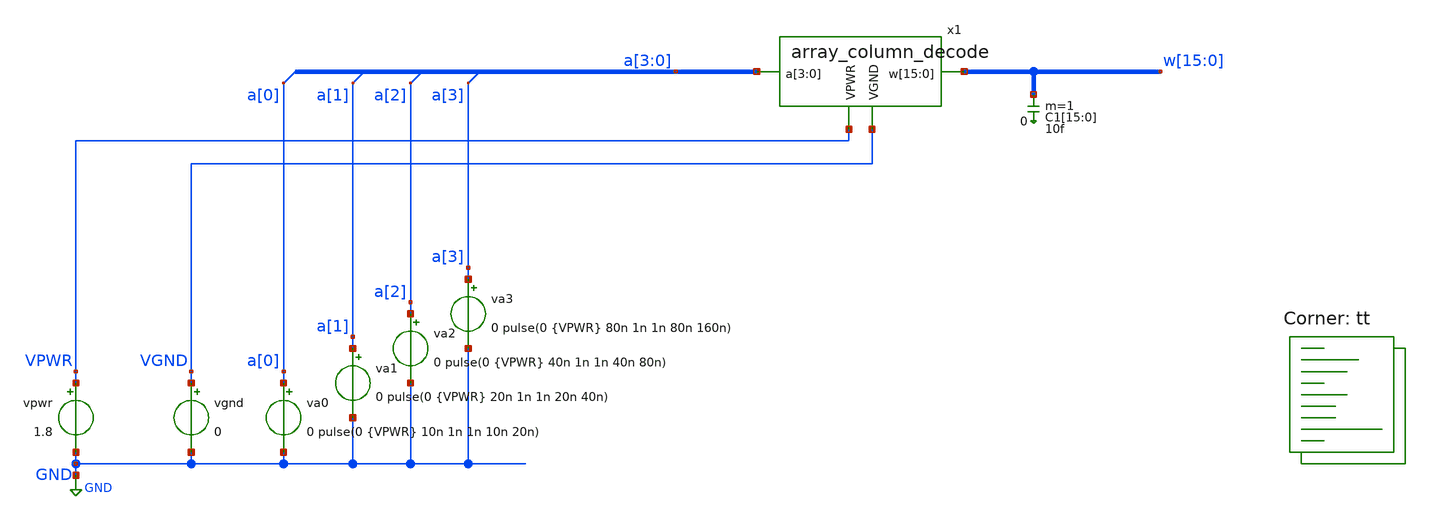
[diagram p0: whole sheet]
** sch_path: xschem/test_array_column_decode.sch
**.subckt test_array_column_decode
vpwr VPWR GND 1.8
va0 a[0] GND 0 pulse(0 {VPWR} 10n 1n 1n 10n 20n)
vgnd VGND GND 0
va1 a[1] GND 0 pulse(0 {VPWR} 20n 1n 1n 20n 40n)
va2 a[2] GND 0 pulse(0 {VPWR} 40n 1n 1n 40n 80n)
va3 a[3] GND 0 pulse(0 {VPWR} 80n 1n 1n 80n 160n)
C1[15] w[15] 0 10f m=1
C1[14] w[14] 0 10f m=1
C1[13] w[13] 0 10f m=1
C1[12] w[12] 0 10f m=1
C1[11] w[11] 0 10f m=1
C1[10] w[10] 0 10f m=1
C1[9] w[9] 0 10f m=1
C1[8] w[8] 0 10f m=1
C1[7] w[7] 0 10f m=1
C1[6] w[6] 0 10f m=1
C1[5] w[5] 0 10f m=1
C1[4] w[4] 0 10f m=1
C1[3] w[3] 0 10f m=1
C1[2] w[2] 0 10f m=1
C1[1] w[1] 0 10f m=1
C1[0] w[0] 0 10f m=1
x1 VPWR VGND a[3] a[2] a[1] a[0] w[15] w[14] w[13] w[12] w[11] w[10] w[9] w[8] w[7] w[6] w[5] w[4]
+ w[3] w[2] w[1] w[0] array_column_decode
**** begin user architecture code
.lib $::SKYWATER_MODELS/sky130.lib.spice tt



.param VPWR=1.8
.param VSS=0
.options savecurrents
.control
  save all
  op
  remzerovec
  write test_array_column_decode.raw
  set appendwrite
  * tran
  tran 1n 1u
  remzerovec
  write test_array_column_decode.raw
.endc



**** end user architecture code
**.ends

* expanding   symbol:  array_column_decode.sym # of pins=4
** sym_path: xschem/array_column_decode.sym
** sch_path: xschem/array_column_decode.sch
.subckt array_column_decode VPWR VGND a[3] a[2] a[1] a[0] w[15] w[14] w[13] w[12] w[11] w[10] w[9]
+ w[8] w[7] w[6] w[5] w[4] w[3] w[2] w[1] w[0]
*.ipin a[3],a[2],a[1],a[0]
*.ipin VPWR
*.ipin VGND
*.opin w[15],w[14],w[13],w[12],w[11],w[10],w[9],w[8],w[7],w[6],w[5],w[4],w[3],w[2],w[1],w[0]
**** begin user architecture code
 .lib $::SKYWATER_MODELS/sky130.lib.spice tt

.include $::SKYWATER_STDCELLS/sky130_fd_sc_hd.spice



**** end user architecture code
x2 a[3] VGND VGND VPWR VPWR a[3]_b sky130_fd_sc_hd__inv_1
x3 a[2] VGND VGND VPWR VPWR a[2]_b sky130_fd_sc_hd__inv_1
x4 a[1] VGND VGND VPWR VPWR a[1]_b sky130_fd_sc_hd__inv_1
x5 a[0] VGND VGND VPWR VPWR a[0]_b sky130_fd_sc_hd__inv_1
x13 a[2] a[3] VGND VGND VPWR VPWR net8 sky130_fd_sc_hd__nand2_2
x6 a[0]_b a[1]_b VGND VGND VPWR VPWR net1 sky130_fd_sc_hd__nand2_2
x7 a[0] a[1]_b VGND VGND VPWR VPWR net3 sky130_fd_sc_hd__nand2_2
x8 a[0]_b a[1] VGND VGND VPWR VPWR net4 sky130_fd_sc_hd__nand2_2
x9 a[0] a[1] VGND VGND VPWR VPWR net5 sky130_fd_sc_hd__nand2_2
x10 a[2]_b a[3]_b VGND VGND VPWR VPWR net2 sky130_fd_sc_hd__nand2_2
x11 a[2] a[3]_b VGND VGND VPWR VPWR net6 sky130_fd_sc_hd__nand2_2
x12 a[2]_b a[3] VGND VGND VPWR VPWR net7 sky130_fd_sc_hd__nand2_2
x14 net1 net2 VGND VGND VGND VPWR VPWR w[0] sky130_fd_sc_hd__nor3_1
x15 net3 net2 VGND VGND VGND VPWR VPWR w[1] sky130_fd_sc_hd__nor3_1
x16 net4 net2 VGND VGND VGND VPWR VPWR w[2] sky130_fd_sc_hd__nor3_1
x17 net5 net2 VGND VGND VGND VPWR VPWR w[3] sky130_fd_sc_hd__nor3_1
x18 net1 net6 VGND VGND VGND VPWR VPWR w[4] sky130_fd_sc_hd__nor3_1
x19 net3 net6 VGND VGND VGND VPWR VPWR w[5] sky130_fd_sc_hd__nor3_1
x20 net4 net6 VGND VGND VGND VPWR VPWR w[6] sky130_fd_sc_hd__nor3_1
x21 net5 net6 VGND VGND VGND VPWR VPWR w[7] sky130_fd_sc_hd__nor3_1
x22 net1 net7 VGND VGND VGND VPWR VPWR w[8] sky130_fd_sc_hd__nor3_1
x23 net3 net7 VGND VGND VGND VPWR VPWR w[9] sky130_fd_sc_hd__nor3_1
x24 net4 net7 VGND VGND VGND VPWR VPWR w[10] sky130_fd_sc_hd__nor3_1
x25 net5 net7 VGND VGND VGND VPWR VPWR w[11] sky130_fd_sc_hd__nor3_1
x26 net1 net8 VGND VGND VGND VPWR VPWR w[12] sky130_fd_sc_hd__nor3_1
x27 net3 net8 VGND VGND VGND VPWR VPWR w[13] sky130_fd_sc_hd__nor3_1
x28 net4 net8 VGND VGND VGND VPWR VPWR w[14] sky130_fd_sc_hd__nor3_1
x29 net5 net8 VGND VGND VGND VPWR VPWR w[15] sky130_fd_sc_hd__nor3_1
x46 VGND VPWR sky130_fd_sc_hd__tapvpwrvgnd_1
x47 VGND VGND VPWR VPWR sky130_fd_sc_hd__decap_3
x48 VGND VPWR sky130_fd_sc_hd__tapvpwrvgnd_1
x49 VGND VPWR sky130_fd_sc_hd__tapvpwrvgnd_1
x50 VGND VGND VPWR VPWR sky130_fd_sc_hd__decap_3
x51 VGND VPWR sky130_fd_sc_hd__tapvpwrvgnd_1
x52 VGND VPWR sky130_fd_sc_hd__tapvpwrvgnd_1
x53 VGND VGND VPWR VPWR sky130_fd_sc_hd__decap_3
x54 VGND VPWR sky130_fd_sc_hd__tapvpwrvgnd_1
x55 VGND VPWR sky130_fd_sc_hd__tapvpwrvgnd_1
x56 VGND VGND VPWR VPWR sky130_fd_sc_hd__decap_3
x57 VGND VPWR sky130_fd_sc_hd__tapvpwrvgnd_1
x58 VGND VPWR sky130_fd_sc_hd__tapvpwrvgnd_1
x59 VGND VGND VPWR VPWR sky130_fd_sc_hd__decap_3
x60 VGND VPWR sky130_fd_sc_hd__tapvpwrvgnd_1
x61 VGND VPWR sky130_fd_sc_hd__tapvpwrvgnd_1
x62 VGND VGND VPWR VPWR sky130_fd_sc_hd__decap_3
x63 VGND VPWR sky130_fd_sc_hd__tapvpwrvgnd_1
x64 VGND VPWR sky130_fd_sc_hd__tapvpwrvgnd_1
x65 VGND VGND VPWR VPWR sky130_fd_sc_hd__decap_3
x66 VGND VPWR sky130_fd_sc_hd__tapvpwrvgnd_1
x67 VGND VPWR sky130_fd_sc_hd__tapvpwrvgnd_1
x68 VGND VGND VPWR VPWR sky130_fd_sc_hd__decap_3
x69 VGND VPWR sky130_fd_sc_hd__tapvpwrvgnd_1
x70 VGND VPWR sky130_fd_sc_hd__tapvpwrvgnd_1
x71 VGND VGND VPWR VPWR sky130_fd_sc_hd__decap_3
x72 VGND VPWR sky130_fd_sc_hd__tapvpwrvgnd_1
x73 VGND VPWR sky130_fd_sc_hd__tapvpwrvgnd_1
x74 VGND VGND VPWR VPWR sky130_fd_sc_hd__decap_3
x75 VGND VPWR sky130_fd_sc_hd__tapvpwrvgnd_1
x76 VGND VPWR sky130_fd_sc_hd__tapvpwrvgnd_1
x77 VGND VGND VPWR VPWR sky130_fd_sc_hd__decap_3
x78 VGND VPWR sky130_fd_sc_hd__tapvpwrvgnd_1
x79 VGND VPWR sky130_fd_sc_hd__tapvpwrvgnd_1
x80 VGND VGND VPWR VPWR sky130_fd_sc_hd__decap_3
x81 VGND VPWR sky130_fd_sc_hd__tapvpwrvgnd_1
x82 VGND VPWR sky130_fd_sc_hd__tapvpwrvgnd_1
x83 VGND VGND VPWR VPWR sky130_fd_sc_hd__decap_3
x84 VGND VPWR sky130_fd_sc_hd__tapvpwrvgnd_1
x85 VGND VPWR sky130_fd_sc_hd__tapvpwrvgnd_1
x86 VGND VGND VPWR VPWR sky130_fd_sc_hd__decap_3
x87 VGND VPWR sky130_fd_sc_hd__tapvpwrvgnd_1
x88 VGND VPWR sky130_fd_sc_hd__tapvpwrvgnd_1
x89 VGND VGND VPWR VPWR sky130_fd_sc_hd__decap_3
x90 VGND VPWR sky130_fd_sc_hd__tapvpwrvgnd_1
x91 VGND VPWR sky130_fd_sc_hd__tapvpwrvgnd_1
x92 VGND VGND VPWR VPWR sky130_fd_sc_hd__decap_3
x93 VGND VPWR sky130_fd_sc_hd__tapvpwrvgnd_1
x142 VGND VPWR sky130_fd_sc_hd__tapvpwrvgnd_1
x143 VGND VGND VPWR VPWR sky130_fd_sc_hd__decap_3
x144 VGND VPWR sky130_fd_sc_hd__tapvpwrvgnd_1
x145 VGND VPWR sky130_fd_sc_hd__tapvpwrvgnd_1
x146 VGND VPWR sky130_fd_sc_hd__tapvpwrvgnd_1
.ends

.GLOBAL GND
.end
